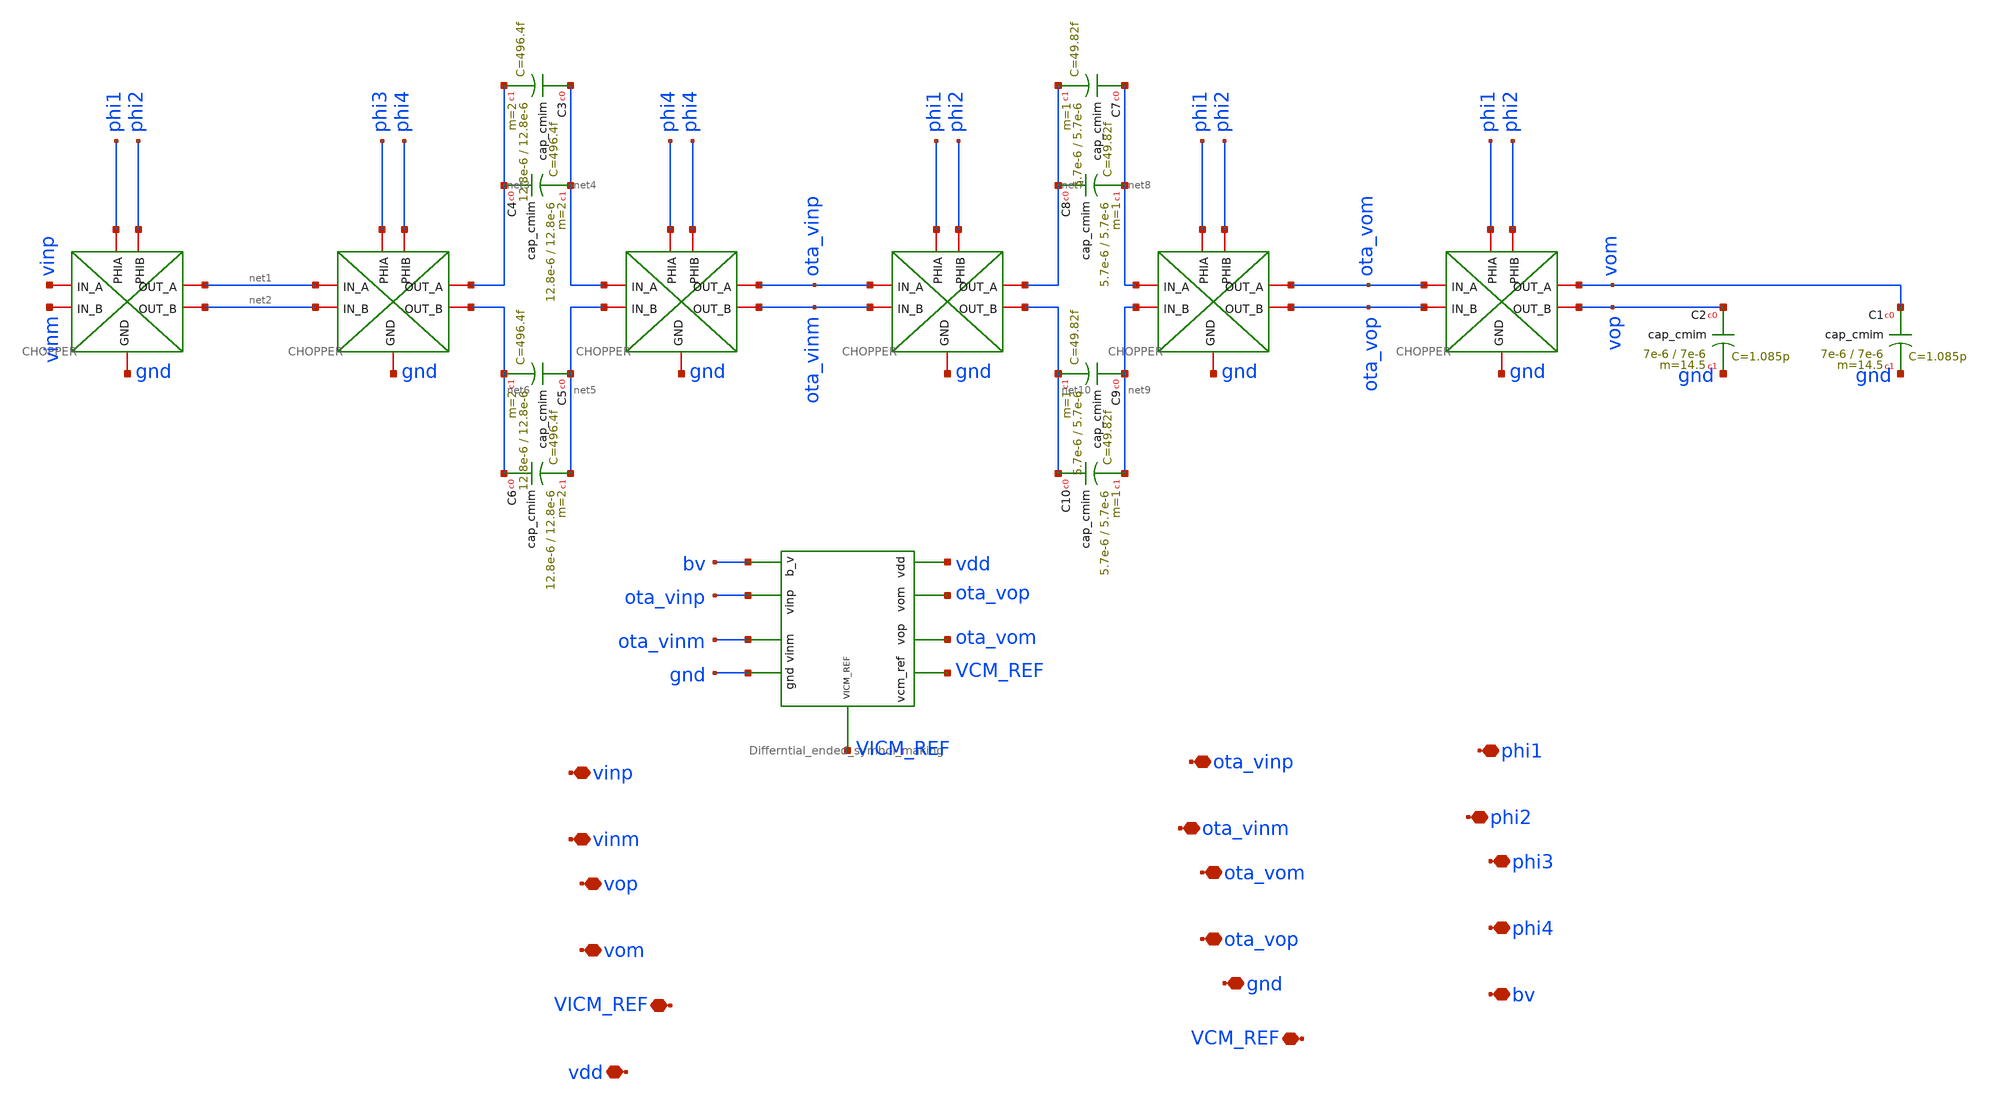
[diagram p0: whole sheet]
** sch_path: imp_boost_tech.sch
**.subckt imp_boost_tech vinp vinm vop vom ota_vinp ota_vinm ota_vom ota_vop phi1 phi2 phi3 phi4
*+ VICM_REF bv gnd vdd VCM_REF
*.iopin vinp
*.iopin vinm
*.iopin vop
*.iopin vom
*.iopin ota_vinp
*.iopin ota_vinm
*.iopin ota_vom
*.iopin ota_vop
*.iopin phi1
*.iopin phi2
*.iopin phi3
*.iopin phi4
*.iopin VICM_REF
*.iopin bv
*.iopin gnd
*.iopin vdd
*.iopin VCM_REF
x1 phi1 net1 vinp phi2 net2 vinm gnd CHOPPER
x3 phi3 net3 net1 phi4 net6 net2 gnd CHOPPER
x4 phi4 ota_vinp net4 phi4 ota_vinm net5 gnd CHOPPER
x5 phi1 net7 ota_vinp phi2 net10 ota_vinm gnd CHOPPER
x6 phi1 ota_vom net8 phi2 ota_vop net9 gnd CHOPPER
x7 phi1 vom ota_vom phi2 vop ota_vop gnd CHOPPER
XC3 net4 net3 cap_cmim w=12.8e-6 l=12.8e-6 m=2 mm_ok=1
XC4 net3 net4 cap_cmim w=12.8e-6 l=12.8e-6 m=2 mm_ok=1
XC5 net5 net6 cap_cmim w=12.8e-6 l=12.8e-6 m=2 mm_ok=1
XC6 net6 net5 cap_cmim w=12.8e-6 l=12.8e-6 m=2 mm_ok=1
XC7 net8 net7 cap_cmim w=5.7e-6 l=5.7e-6 m=1 mm_ok=1
XC8 net7 net8 cap_cmim w=5.7e-6 l=5.7e-6 m=1 mm_ok=1
XC9 net9 net10 cap_cmim w=5.7e-6 l=5.7e-6 m=1 mm_ok=1
XC10 net10 net9 cap_cmim w=5.7e-6 l=5.7e-6 m=1 mm_ok=1
x2 vdd VCM_REF ota_vop ota_vom gnd bv ota_vinm ota_vinp VICM_REF Differntial_ended_symbol_making
XC1 vom gnd cap_cmim w=7e-6 l=7e-6 m=14.5 mm_ok=1
XC2 vop gnd cap_cmim w=7e-6 l=7e-6 m=14.5 mm_ok=1
**.ends
.end
